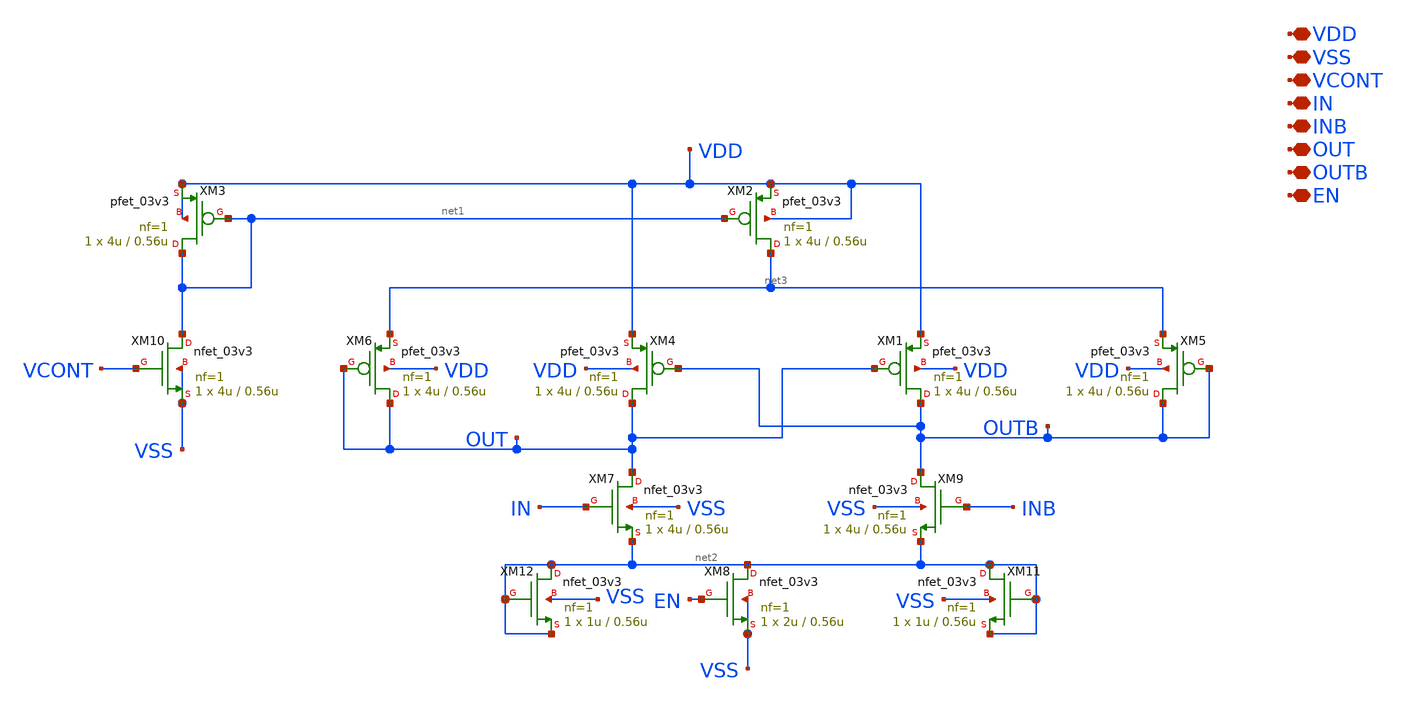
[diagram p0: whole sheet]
** sch_path: Clock_Generator_PAKISTAN_02/Schematics/Delay_Cell.sch
**.subckt Delay_Cell VDD VSS VCONT IN INB OUT OUTB EN
*.iopin VDD
*.iopin VSS
*.iopin VCONT
*.iopin IN
*.iopin INB
*.iopin OUT
*.iopin OUTB
*.iopin EN
XM1 OUTB OUT VDD VDD pfet_03v3 L=0.56u W=4u nf=1 ad='int((nf+1)/2) * W/nf * 0.18u' as='int((nf+2)/2) * W/nf * 0.18u'
+ pd='2*int((nf+1)/2) * (W/nf + 0.18u)' ps='2*int((nf+2)/2) * (W/nf + 0.18u)' nrd='0.18u / W' nrs='0.18u / W'
+ sa=0 sb=0 sd=0 m=1
XM2 net3 net1 VDD VDD pfet_03v3 L=0.56u W=4u nf=1 ad='int((nf+1)/2) * W/nf * 0.18u' as='int((nf+2)/2) * W/nf * 0.18u'
+ pd='2*int((nf+1)/2) * (W/nf + 0.18u)' ps='2*int((nf+2)/2) * (W/nf + 0.18u)' nrd='0.18u / W' nrs='0.18u / W'
+ sa=0 sb=0 sd=0 m=1
XM4 OUT OUTB VDD VDD pfet_03v3 L=0.56u W=4u nf=1 ad='int((nf+1)/2) * W/nf * 0.18u' as='int((nf+2)/2) * W/nf * 0.18u'
+ pd='2*int((nf+1)/2) * (W/nf + 0.18u)' ps='2*int((nf+2)/2) * (W/nf + 0.18u)' nrd='0.18u / W' nrs='0.18u / W'
+ sa=0 sb=0 sd=0 m=1
XM5 OUTB OUTB net3 VDD pfet_03v3 L=0.56u W=4u nf=1 ad='int((nf+1)/2) * W/nf * 0.18u' as='int((nf+2)/2) * W/nf * 0.18u'
+ pd='2*int((nf+1)/2) * (W/nf + 0.18u)' ps='2*int((nf+2)/2) * (W/nf + 0.18u)' nrd='0.18u / W' nrs='0.18u / W'
+ sa=0 sb=0 sd=0 m=1
XM6 OUT OUT net3 VDD pfet_03v3 L=0.56u W=4u nf=1 ad='int((nf+1)/2) * W/nf * 0.18u' as='int((nf+2)/2) * W/nf * 0.18u'
+ pd='2*int((nf+1)/2) * (W/nf + 0.18u)' ps='2*int((nf+2)/2) * (W/nf + 0.18u)' nrd='0.18u / W' nrs='0.18u / W'
+ sa=0 sb=0 sd=0 m=1
XM7 OUT IN net2 VSS nfet_03v3 L=0.56u W=4u nf=1 ad='int((nf+1)/2) * W/nf * 0.18u' as='int((nf+2)/2) * W/nf * 0.18u'
+ pd='2*int((nf+1)/2) * (W/nf + 0.18u)' ps='2*int((nf+2)/2) * (W/nf + 0.18u)' nrd='0.18u / W' nrs='0.18u / W'
+ sa=0 sb=0 sd=0 m=1
XM9 OUTB INB net2 VSS nfet_03v3 L=0.56u W=4u nf=1 ad='int((nf+1)/2) * W/nf * 0.18u' as='int((nf+2)/2) * W/nf * 0.18u'
+ pd='2*int((nf+1)/2) * (W/nf + 0.18u)' ps='2*int((nf+2)/2) * (W/nf + 0.18u)' nrd='0.18u / W' nrs='0.18u / W'
+ sa=0 sb=0 sd=0 m=1
XM3 net1 net1 VDD VDD pfet_03v3 L=0.56u W=4u nf=1 ad='int((nf+1)/2) * W/nf * 0.18u' as='int((nf+2)/2) * W/nf * 0.18u'
+ pd='2*int((nf+1)/2) * (W/nf + 0.18u)' ps='2*int((nf+2)/2) * (W/nf + 0.18u)' nrd='0.18u / W' nrs='0.18u / W'
+ sa=0 sb=0 sd=0 m=1
XM10 net1 VCONT VSS VSS nfet_03v3 L=0.56u W=4u nf=1 ad='int((nf+1)/2) * W/nf * 0.18u' as='int((nf+2)/2) * W/nf * 0.18u'
+ pd='2*int((nf+1)/2) * (W/nf + 0.18u)' ps='2*int((nf+2)/2) * (W/nf + 0.18u)' nrd='0.18u / W' nrs='0.18u / W'
+ sa=0 sb=0 sd=0 m=1
XM8 net2 EN VSS VSS nfet_03v3 L=0.56u W=2u nf=1 ad='int((nf+1)/2) * W/nf * 0.18u' as='int((nf+2)/2) * W/nf * 0.18u'
+ pd='2*int((nf+1)/2) * (W/nf + 0.18u)' ps='2*int((nf+2)/2) * (W/nf + 0.18u)' nrd='0.18u / W' nrs='0.18u / W'
+ sa=0 sb=0 sd=0 m=1
XM11 net2 net2 net2 VSS nfet_03v3 L=0.56u W=1u nf=1 ad='int((nf+1)/2) * W/nf * 0.18u' as='int((nf+2)/2) * W/nf * 0.18u'
+ pd='2*int((nf+1)/2) * (W/nf + 0.18u)' ps='2*int((nf+2)/2) * (W/nf + 0.18u)' nrd='0.18u / W' nrs='0.18u / W'
+ sa=0 sb=0 sd=0 m=1
XM12 net2 net2 net2 VSS nfet_03v3 L=0.56u W=1u nf=1 ad='int((nf+1)/2) * W/nf * 0.18u' as='int((nf+2)/2) * W/nf * 0.18u'
+ pd='2*int((nf+1)/2) * (W/nf + 0.18u)' ps='2*int((nf+2)/2) * (W/nf + 0.18u)' nrd='0.18u / W' nrs='0.18u / W'
+ sa=0 sb=0 sd=0 m=1
**.ends
.end
